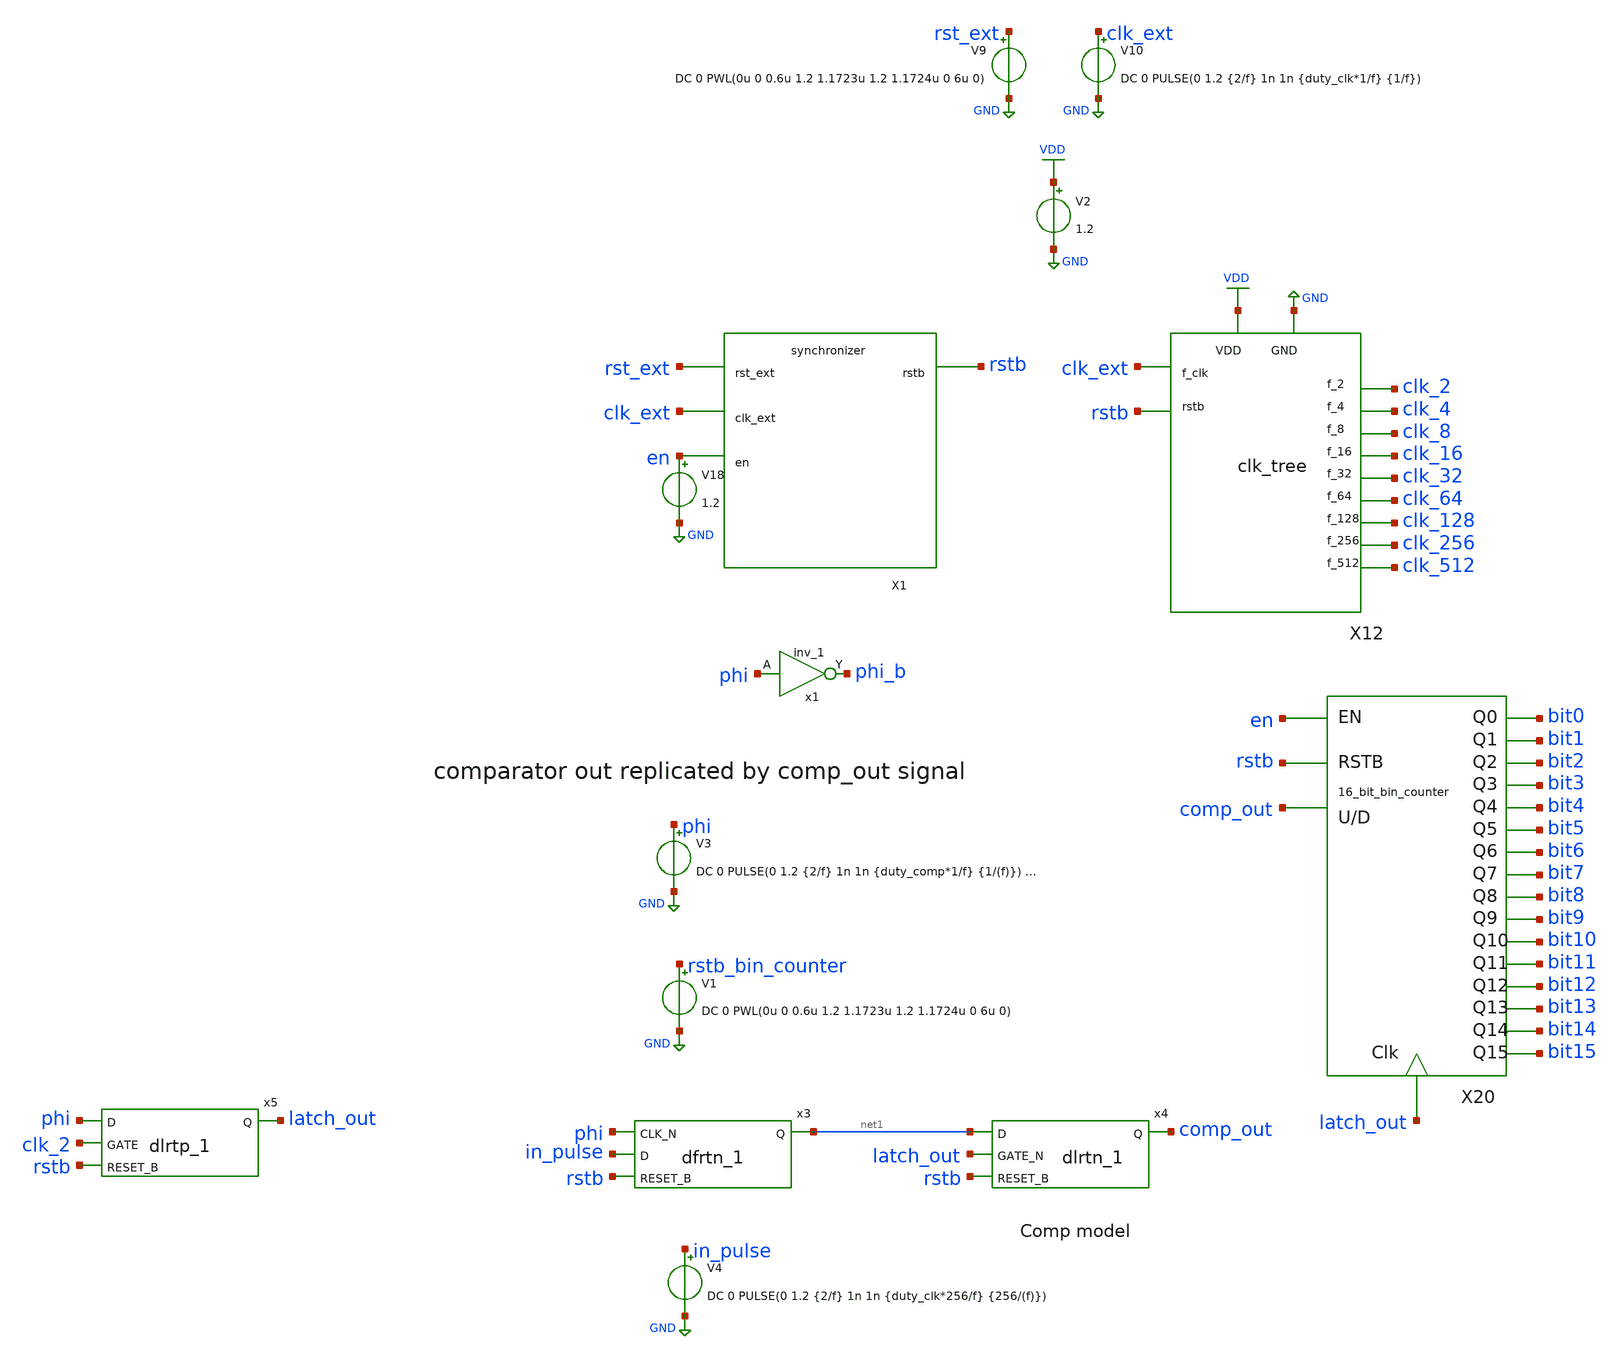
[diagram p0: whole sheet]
** sch_path: xschem/archive/gray selector/test.sch
**.subckt test
V2 VDD GND 1.2
V10 clk_ext GND DC 0 PULSE(0 1.2 {2/f} 1n 1n {duty_clk*1/f} {1/f})
V9 rst_ext GND DC 0 PWL(0u 0 0.6u 1.2 1.1723u 1.2 1.1724u 0 6u 0)
X12 rstb clk_ext clk_2 clk_4 clk_8 clk_16 clk_32 clk_64 clk_128 clk_256 clk_512 VDD GND clk_tree
X1 rst_ext clk_ext en rstb synchronizer
V18 en GND 1.2
X20 en bit1 bit6 latch_out bit0 bit2 bit3 bit4 bit5 bit7 bit8 bit9 bit10 bit11 bit12 bit13 bit14
+ bit15 rstb comp_out bin_counter
V3 phi GND DC 0 PULSE(0 1.2 {2/f} 1n 1n {duty_comp*1/f} {1/(f)}) -18
V1 rstb_bin_counter GND DC 0 PWL(0u 0 0.6u 1.2 1.1723u 1.2 1.1724u 0 6u 0)
x1 phi GND GND VDD VDD phi_b sky130_fd_sc_lp__inv_1
V4 in_pulse GND DC 0 PULSE(0 1.2 {2/f} 1n 1n {duty_clk*256/f} {256/(f)})
x4 net1 latch_out rstb GND GND VDD VDD comp_out sky130_fd_sc_lp__dlrtn_1
x5 phi clk_2 rstb GND GND VDD VDD latch_out sky130_fd_sc_lp__dlrtp_1
x3 phi in_pulse rstb GND GND VDD VDD net1 sky130_fd_sc_lp__dfrtn_1
**** begin user architecture code


.lib /home/sky/sky130A/libs.tech/ngspice/sky130.lib.spice tt
.include /home/sky/sky130A/libs.ref/sky130_fd_sc_lp/spice/sky130_fd_sc_lp.spice
.options abstol=1e-14 reltol=1e-4
.param f=2560k
.param duty_clk=0.5
.param duty_comp=0.45
*.ic v(out)=0
.tran {(1/100)*(1/f)} {256/f}
.save all


**** end user architecture code
**.ends
.GLOBAL VDD
.GLOBAL GND
.end
